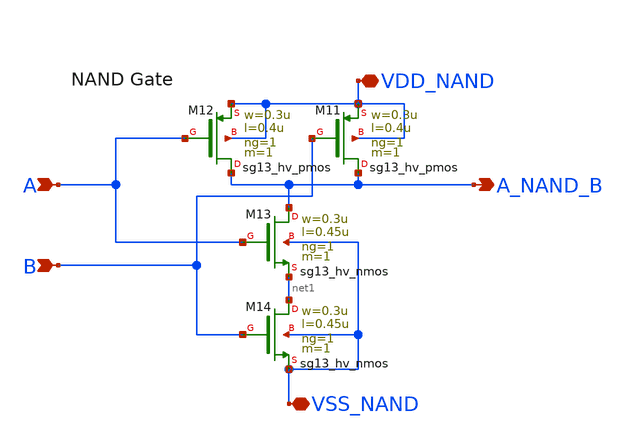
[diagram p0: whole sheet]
** sch_path: circuit_files/sar_adc_20260903/nand2.sch
**.subckt nand2 A_NAND_B A B VDD_NAND VSS_NAND
*.opin A_NAND_B
*.ipin A
*.ipin B
*.iopin VDD_NAND
*.iopin VSS_NAND
XM11 A_NAND_B B VDD_NAND VDD_NAND sg13_hv_pmos w=0.3u l=0.4u ng=1 m=1 mm_ok=1
XM12 A_NAND_B A VDD_NAND VDD_NAND sg13_hv_pmos w=0.3u l=0.4u ng=1 m=1 mm_ok=1
XM13 A_NAND_B A net1 VSS_NAND sg13_hv_nmos w=0.3u l=0.45u ng=1 m=1 mm_ok=1
XM14 net1 B VSS_NAND VSS_NAND sg13_hv_nmos w=0.3u l=0.45u ng=1 m=1 mm_ok=1
**.ends
.end
